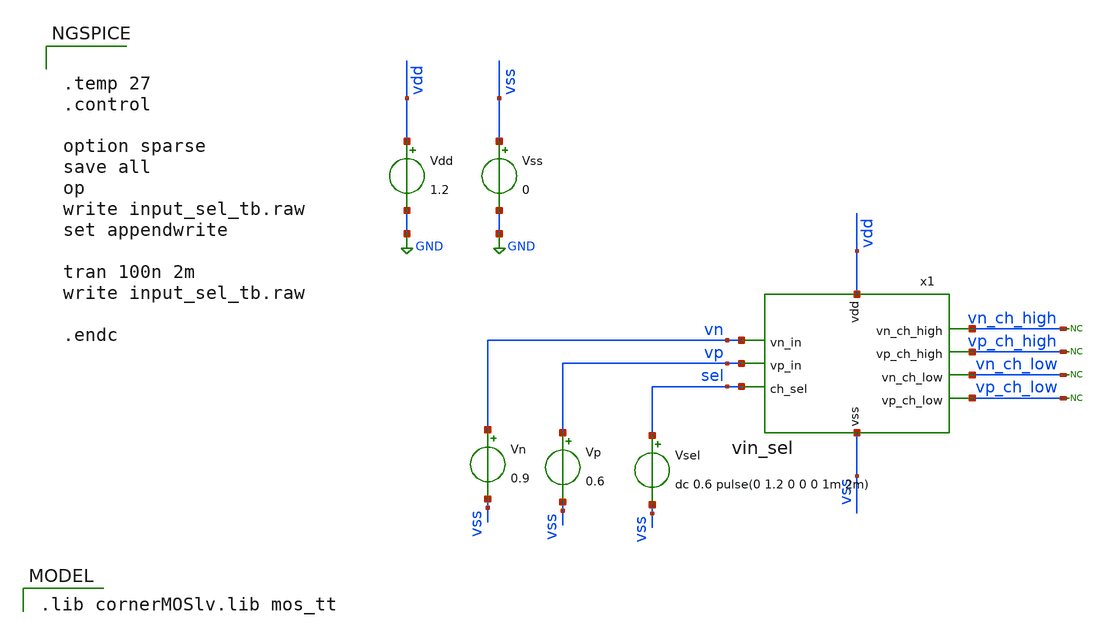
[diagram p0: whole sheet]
** sch_path: v2_feature_extr_withf/vin_sel_tb.sch
**.subckt vin_sel_tb
x1 vn vdd vss vp sel vn_ch_high vp_ch_high vn_ch_low vp_ch_low vin_sel
Vdd vdd GND 1.2
Vss vss GND 0
* noconn vn_ch_high
* noconn vp_ch_high
* noconn vn_ch_low
* noconn vp_ch_low
Vsel sel vss dc 0.6 pulse(0 1.2 0 0 0 1m 2m)
Vp vp vss 0.6
Vn vn vss 0.9
**** begin user architecture code


.temp 27
.control

option sparse
save all
op
write input_sel_tb.raw
set appendwrite

tran 100n 2m
write input_sel_tb.raw

.endc


 .lib cornerMOSlv.lib mos_tt

**** end user architecture code
**.ends
.GLOBAL GND
.end
